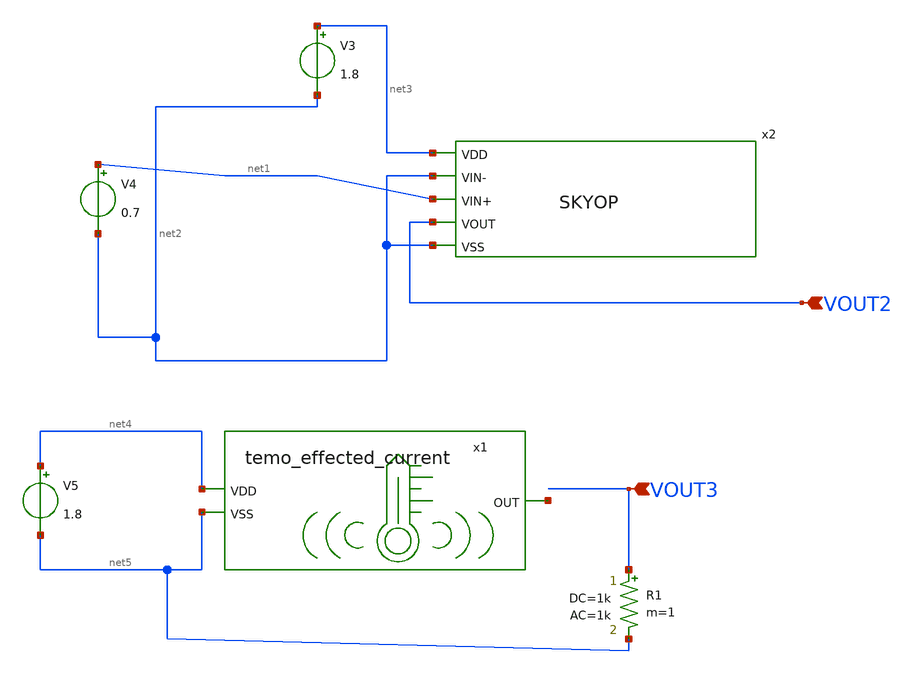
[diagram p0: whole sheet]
** sch_path: design/JNW_GR01_SKY130A/TB_OP6.sch
**.subckt TB_OP6 VOUT2 VOUT3
*.ipin VOUT2
*.ipin VOUT3
V3 net3 net2 1.8
V4 net1 net2 0.7
x2 net3 net2 net1 VOUT2 net2 SKYOP
V5 net4 net5 1.8
R1 VOUT3 net5 1k ac=1k m=1
x1 net4 net6 net5 temo_effected_current
**.ends
.end
